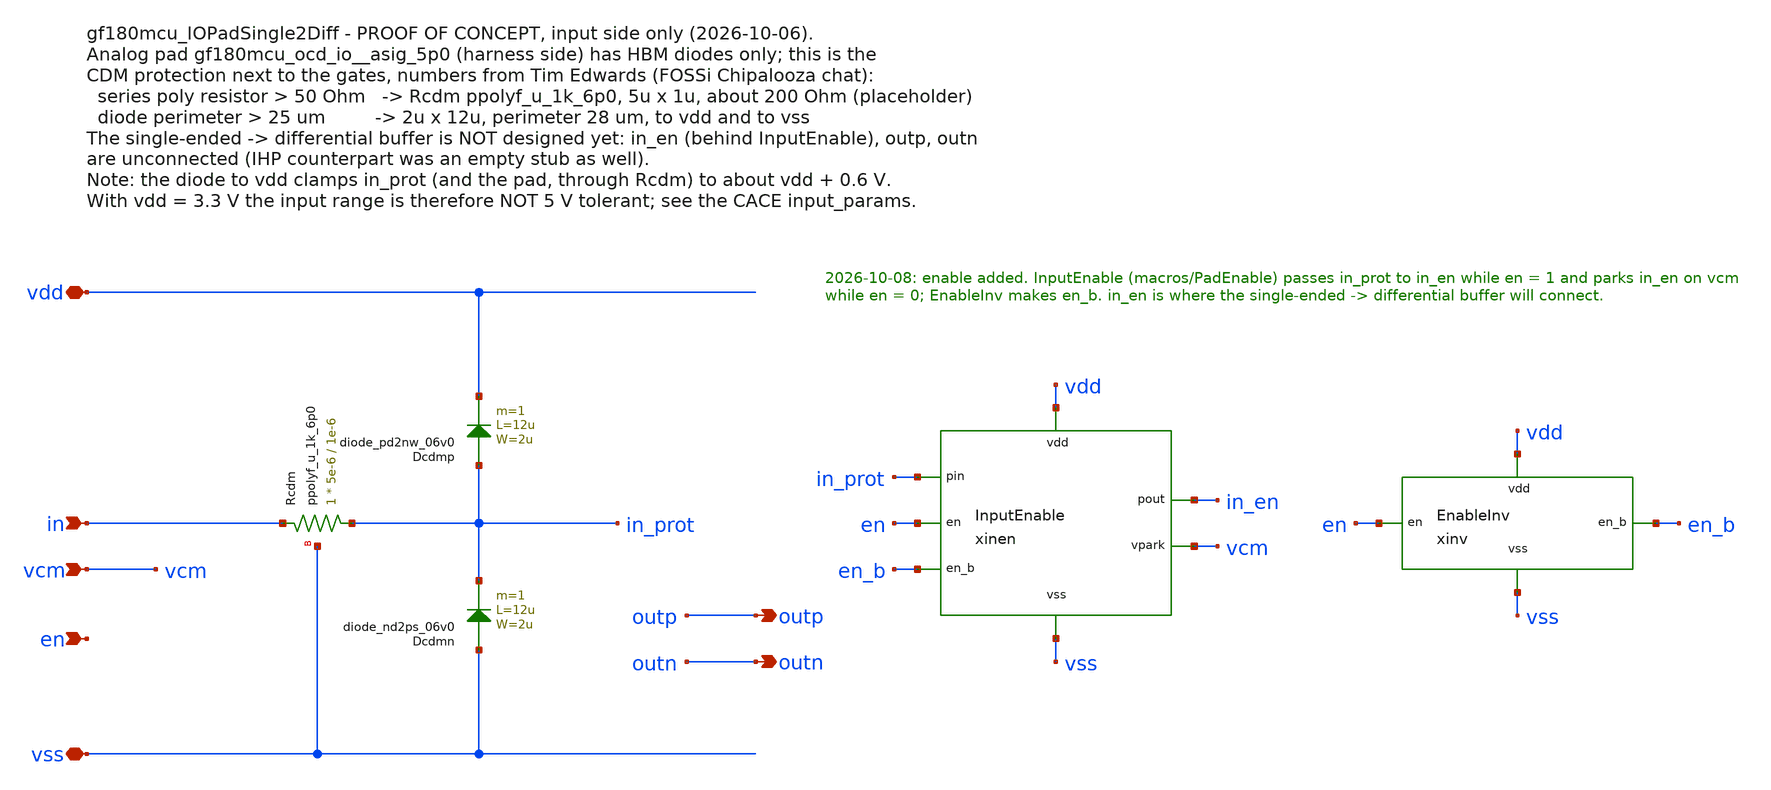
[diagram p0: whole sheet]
** sch_path: macros/gf180mcu_IOPadSingle2Diff/schematic/xschem/gf180mcu_IOPadSingle2Diff.sch
**.subckt gf180mcu_IOPadSingle2Diff vdd outp vcm in outn vss en
*.iopin vdd
*.opin outp
*.ipin vcm
*.ipin in
*.opin outn
*.iopin vss
*.ipin en
XRcdm in_prot in vss ppolyf_u_1k_6p0 r_width=5e-6 r_length=1e-6 m=1
Dcdmp in_prot vdd diode_pd2nw_06v0 area='2u * 12u ' pj='2*2u + 2*12u ' m=1
Dcdmn vss in_prot diode_nd2ps_06v0 area='2u * 12u ' pj='2*2u + 2*12u ' m=1
xinen vdd vss en en_b in_prot in_en vcm InputEnable
xinv vdd vss en en_b EnableInv
**.ends

* expanding   symbol:  InputEnable.sym # of pins=7
** sym_path: macros/PadEnable/schematic/xschem/InputEnable.sym
** sch_path: macros/PadEnable/schematic/xschem/InputEnable.sch
.subckt InputEnable vdd vss en en_b pin pout vpark
*.iopin vdd
*.iopin vss
*.ipin en
*.ipin en_b
*.iopin pin
*.iopin pout
*.ipin vpark
XTGP1 pout en_b pin vdd pfet_03v3 L=0.5u W=4u nf=1 ad='int((nf+1)/2) * W/nf * 0.18u' as='int((nf+2)/2) * W/nf * 0.18u'
+ pd='2*int((nf+1)/2) * (W/nf + 0.18u)' ps='2*int((nf+2)/2) * (W/nf + 0.18u)' nrd='0.18u / W' nrs='0.18u / W'
+ sa=0 sb=0 sd=0 m=1
XTGN1 pin en pout vss nfet_03v3 L=0.5u W=4u nf=1 ad='int((nf+1)/2) * W/nf * 0.18u' as='int((nf+2)/2) * W/nf * 0.18u'
+ pd='2*int((nf+1)/2) * (W/nf + 0.18u)' ps='2*int((nf+2)/2) * (W/nf + 0.18u)' nrd='0.18u / W' nrs='0.18u / W'
+ sa=0 sb=0 sd=0 m=1
XTGP2 vpark en pout vdd pfet_03v3 L=0.5u W=4u nf=1 ad='int((nf+1)/2) * W/nf * 0.18u' as='int((nf+2)/2) * W/nf * 0.18u'
+ pd='2*int((nf+1)/2) * (W/nf + 0.18u)' ps='2*int((nf+2)/2) * (W/nf + 0.18u)' nrd='0.18u / W' nrs='0.18u / W'
+ sa=0 sb=0 sd=0 m=1
XTGN2 pout en_b vpark vss nfet_03v3 L=0.5u W=4u nf=1 ad='int((nf+1)/2) * W/nf * 0.18u' as='int((nf+2)/2) * W/nf * 0.18u'
+ pd='2*int((nf+1)/2) * (W/nf + 0.18u)' ps='2*int((nf+2)/2) * (W/nf + 0.18u)' nrd='0.18u / W' nrs='0.18u / W'
+ sa=0 sb=0 sd=0 m=1
.ends


* expanding   symbol:  EnableInv.sym # of pins=4
** sym_path: macros/PadEnable/schematic/xschem/EnableInv.sym
** sch_path: macros/PadEnable/schematic/xschem/EnableInv.sch
.subckt EnableInv vdd vss en en_b
*.iopin vdd
*.iopin vss
*.ipin en
*.opin en_b
XMP en_b en vdd vdd pfet_03v3 L=0.5u W=2u nf=1 ad='int((nf+1)/2) * W/nf * 0.18u' as='int((nf+2)/2) * W/nf * 0.18u'
+ pd='2*int((nf+1)/2) * (W/nf + 0.18u)' ps='2*int((nf+2)/2) * (W/nf + 0.18u)' nrd='0.18u / W' nrs='0.18u / W'
+ sa=0 sb=0 sd=0 m=1
XMN en_b en vss vss nfet_03v3 L=0.5u W=1u nf=1 ad='int((nf+1)/2) * W/nf * 0.18u' as='int((nf+2)/2) * W/nf * 0.18u'
+ pd='2*int((nf+1)/2) * (W/nf + 0.18u)' ps='2*int((nf+2)/2) * (W/nf + 0.18u)' nrd='0.18u / W' nrs='0.18u / W'
+ sa=0 sb=0 sd=0 m=1
.ends

.end
